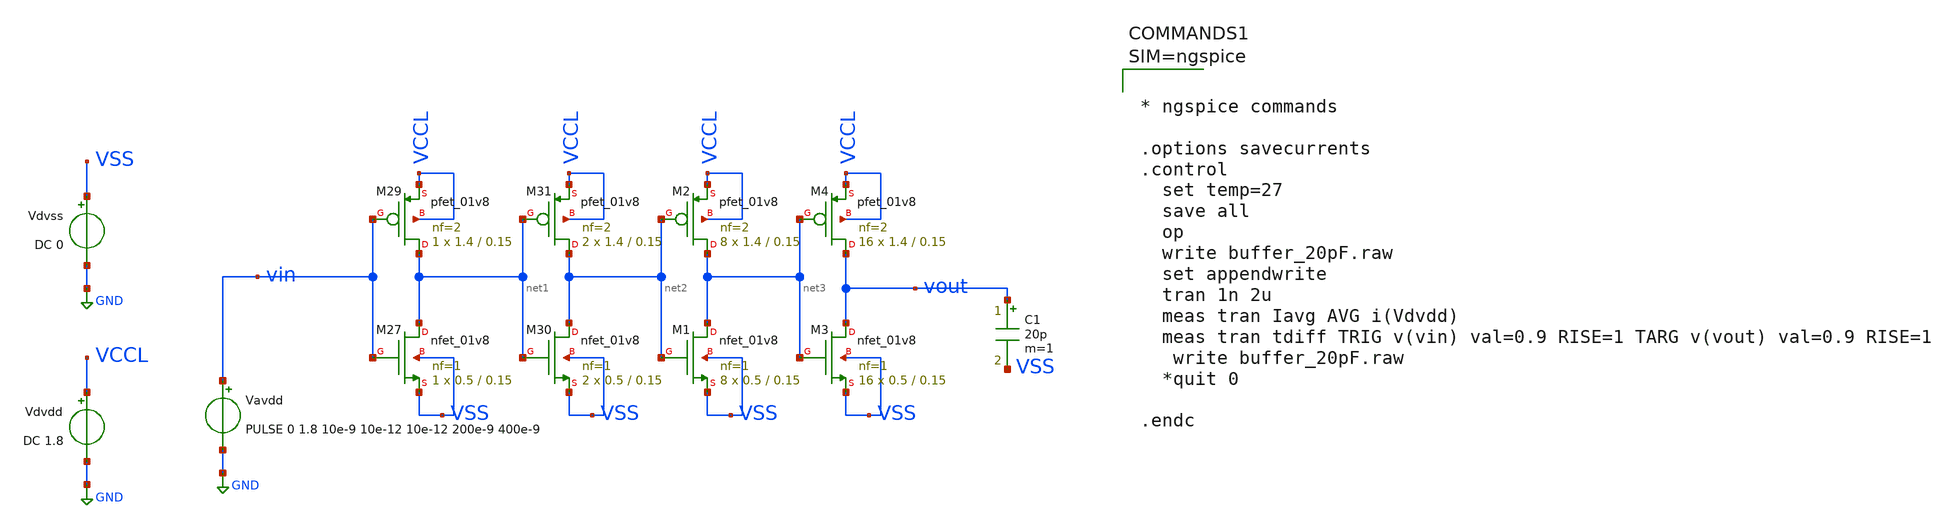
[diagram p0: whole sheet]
** sch_path: xschem/buffer_20pF.sch
**.subckt buffer_20pF
Vdvss VSS GND DC 0
XM27 net1 vin VSS VSS sky130_fd_pr__nfet_01v8 L=0.15 W=0.5 nf=1 ad='int((nf+1)/2) * W/nf * 0.29' as='int((nf+2)/2) * W/nf * 0.29'
+ pd='2*int((nf+1)/2) * (W/nf + 0.29)' ps='2*int((nf+2)/2) * (W/nf + 0.29)' nrd='0.29 / W' nrs='0.29 / W'
+ sa=0 sb=0 sd=0 mult=1 m=1
XM29 net1 vin VCCL VCCL sky130_fd_pr__pfet_01v8 L=0.15 W=1.4 nf=2 ad='int((nf+1)/2) * W/nf * 0.29' as='int((nf+2)/2) * W/nf * 0.29'
+ pd='2*int((nf+1)/2) * (W/nf + 0.29)' ps='2*int((nf+2)/2) * (W/nf + 0.29)' nrd='0.29 / W' nrs='0.29 / W'
+ sa=0 sb=0 sd=0 mult=1 m=1
XM30 net2 net1 VSS VSS sky130_fd_pr__nfet_01v8 L=0.15 W=0.5 nf=1 ad='int((nf+1)/2) * W/nf * 0.29' as='int((nf+2)/2) * W/nf * 0.29'
+ pd='2*int((nf+1)/2) * (W/nf + 0.29)' ps='2*int((nf+2)/2) * (W/nf + 0.29)' nrd='0.29 / W' nrs='0.29 / W'
+ sa=0 sb=0 sd=0 mult=2 m=2
XM31 net2 net1 VCCL VCCL sky130_fd_pr__pfet_01v8 L=0.15 W=1.4 nf=2 ad='int((nf+1)/2) * W/nf * 0.29' as='int((nf+2)/2) * W/nf * 0.29'
+ pd='2*int((nf+1)/2) * (W/nf + 0.29)' ps='2*int((nf+2)/2) * (W/nf + 0.29)' nrd='0.29 / W' nrs='0.29 / W'
+ sa=0 sb=0 sd=0 mult=2 m=2
Vdvdd VCCL GND DC 1.8
Vavdd vin GND PULSE 0 1.8 10e-9 10e-12 10e-12 200e-9 400e-9
C1 vout VSS 20p m=1
XM1 net3 net2 VSS VSS sky130_fd_pr__nfet_01v8 L=0.15 W=0.5 nf=1 ad='int((nf+1)/2) * W/nf * 0.29' as='int((nf+2)/2) * W/nf * 0.29'
+ pd='2*int((nf+1)/2) * (W/nf + 0.29)' ps='2*int((nf+2)/2) * (W/nf + 0.29)' nrd='0.29 / W' nrs='0.29 / W'
+ sa=0 sb=0 sd=0 mult=8 m=8
XM2 net3 net2 VCCL VCCL sky130_fd_pr__pfet_01v8 L=0.15 W=1.4 nf=2 ad='int((nf+1)/2) * W/nf * 0.29' as='int((nf+2)/2) * W/nf * 0.29'
+ pd='2*int((nf+1)/2) * (W/nf + 0.29)' ps='2*int((nf+2)/2) * (W/nf + 0.29)' nrd='0.29 / W' nrs='0.29 / W'
+ sa=0 sb=0 sd=0 mult=8 m=8
XM3 vout net3 VSS VSS sky130_fd_pr__nfet_01v8 L=0.15 W=0.5 nf=1 ad='int((nf+1)/2) * W/nf * 0.29' as='int((nf+2)/2) * W/nf * 0.29'
+ pd='2*int((nf+1)/2) * (W/nf + 0.29)' ps='2*int((nf+2)/2) * (W/nf + 0.29)' nrd='0.29 / W' nrs='0.29 / W'
+ sa=0 sb=0 sd=0 mult=16 m=16
XM4 vout net3 VCCL VCCL sky130_fd_pr__pfet_01v8 L=0.15 W=1.4 nf=2 ad='int((nf+1)/2) * W/nf * 0.29' as='int((nf+2)/2) * W/nf * 0.29'
+ pd='2*int((nf+1)/2) * (W/nf + 0.29)' ps='2*int((nf+2)/2) * (W/nf + 0.29)' nrd='0.29 / W' nrs='0.29 / W'
+ sa=0 sb=0 sd=0 mult=16 m=16
**** begin user architecture code
 .lib $::SKYWATER_MODELS/sky130.lib.spice tt

.include $::SKYWATER_STDCELLS/sky130_fd_sc_hd.spice
.include $::SKYWATER_STDCELLS/../../sky130_fd_sc_hvl/spice/sky130_fd_sc_hvl.spice





* ngspice commands

.options savecurrents
.control
  set temp=27
  save all
  op
  write buffer_20pF.raw
  set appendwrite
  tran 1n 2u
  meas tran Iavg AVG i(Vdvdd)
  meas tran tdiff TRIG v(vin) val=0.9 RISE=1 TARG v(vout) val=0.9 RISE=1
   write buffer_20pF.raw
  *quit 0

.endc



**** end user architecture code
**.ends
.GLOBAL GND
.end
